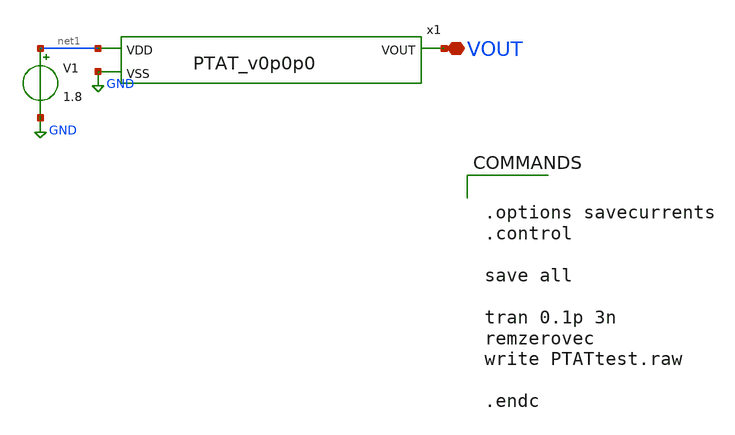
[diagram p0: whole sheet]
** sch_path: PTAT/xschem/PTATtest.sch
.lib $::SKYWATER_MODELS/sky130.lib.spice tt
.include $::SKYWATER_STDCELLS/sky130_fd_sc_hd.spice

**.subckt PTATtest VOUT
*.iopin VOUT
V1 net1 GND 1.8
x1 net1 VOUT GND PTAT_v0p0p0
**** begin user architecture code


.options savecurrents
.control

save all

tran 0.1p 3n
remzerovec
write PTATtest.raw

.endc


**** end user architecture code
**.ends
.GLOBAL GND
.end
